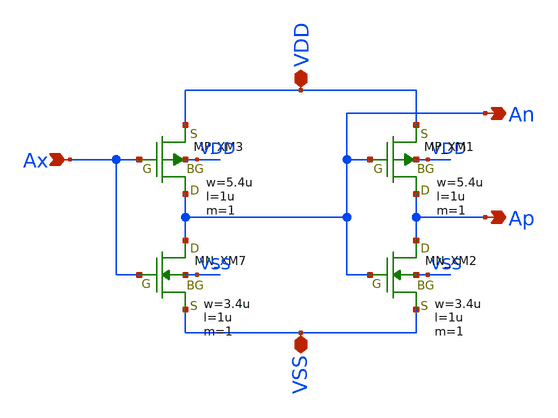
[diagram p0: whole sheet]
** sch_path: module/SRAM128/schematic/ADB.sch
**.subckt ADB Ap Ax VDD VSS An
*.opin Ap
*.ipin Ax
*.iopin VDD
*.iopin VSS
*.opin An
XXM3 An Ax VDD VDD PMOS w=5.4u l=1u as=0 ad=0 ps=0 pd=0 nrd=0 nrs=0 m=1
XXM7 An Ax VSS VSS NMOS w=3.4u l=1u as=0 ad=0 ps=0 pd=0 nrd=0 nrs=0 m=1
XXM1 Ap An VDD VDD PMOS w=5.4u l=1u as=0 ad=0 ps=0 pd=0 nrd=0 nrs=0 m=1
XXM2 Ap An VSS VSS NMOS w=3.4u l=1u as=0 ad=0 ps=0 pd=0 nrd=0 nrs=0 m=1
**.ends
.end
